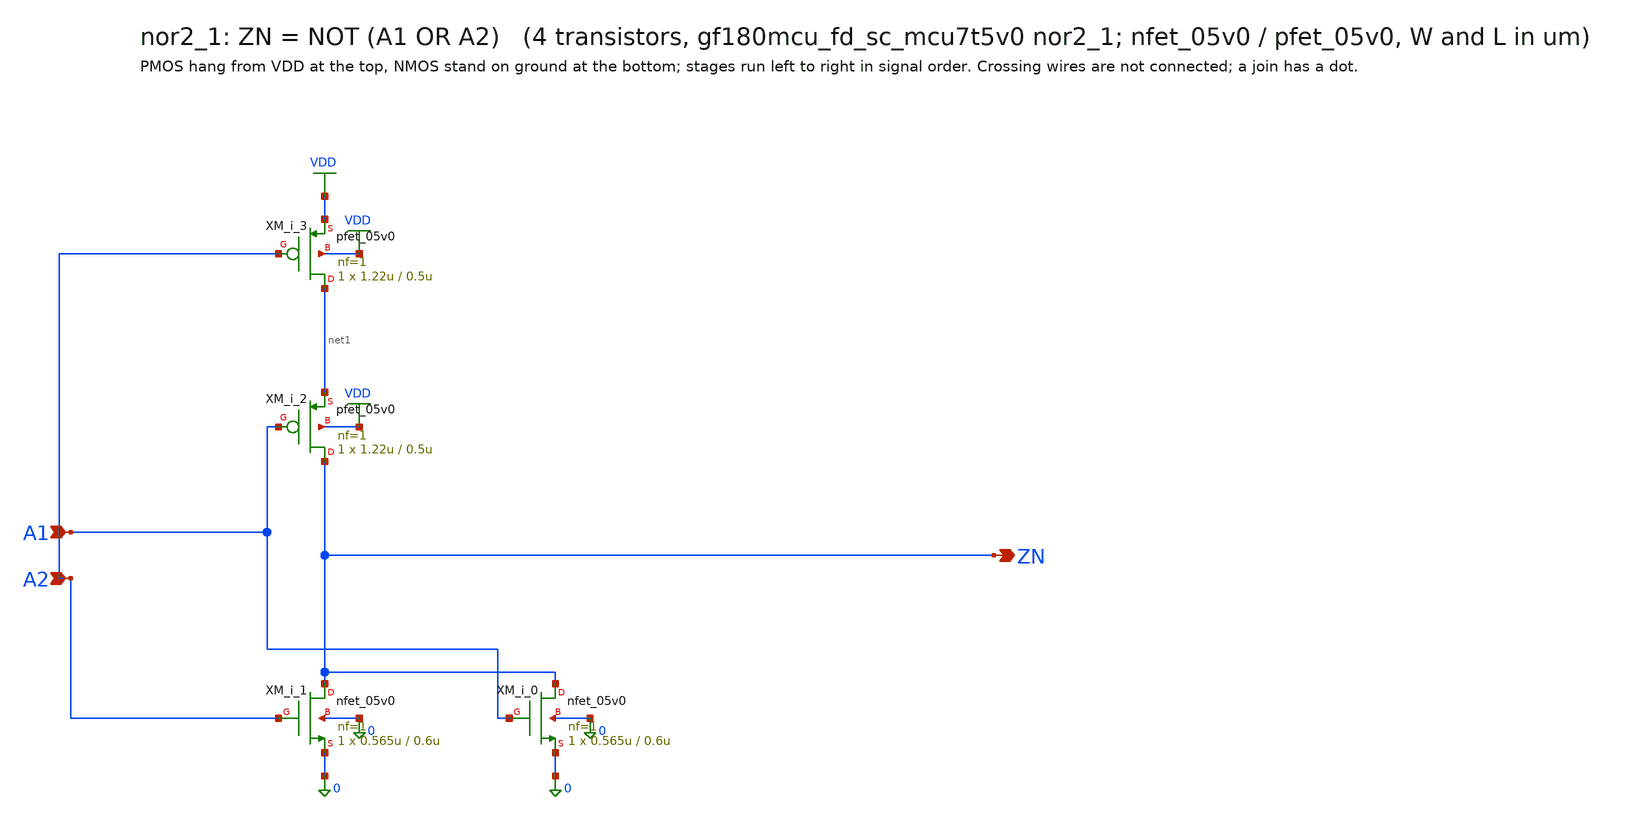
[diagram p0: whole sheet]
** sch_path: xschem/cells_tx/nor2_1.sch
**.subckt nor2_1 A1 A2 ZN
*.ipin A1
*.ipin A2
*.opin ZN
XM_i_1 ZN A2 0 0 nfet_05v0 L=0.6u W=0.565u nf=1 ad=2.825e-13 as=2.825e-13 pd=2.13e-06 ps=2.13e-06
+ nrd=0 nrs=0 sa=0 sb=0 sd=0 m=1
XM_i_0 ZN A1 0 0 nfet_05v0 L=0.6u W=0.565u nf=1 ad=2.825e-13 as=2.825e-13 pd=2.13e-06 ps=2.13e-06
+ nrd=0 nrs=0 sa=0 sb=0 sd=0 m=1
XM_i_3 net1 A2 VDD VDD pfet_05v0 L=0.5u W=1.22u nf=1 ad=6.1e-13 as=6.1e-13 pd=3.44e-06 ps=3.44e-06
+ nrd=0 nrs=0 sa=0 sb=0 sd=0 m=1
XM_i_2 ZN A1 net1 VDD pfet_05v0 L=0.5u W=1.22u nf=1 ad=6.1e-13 as=6.1e-13 pd=3.44e-06 ps=3.44e-06
+ nrd=0 nrs=0 sa=0 sb=0 sd=0 m=1
**.ends
.GLOBAL VDD
.end
